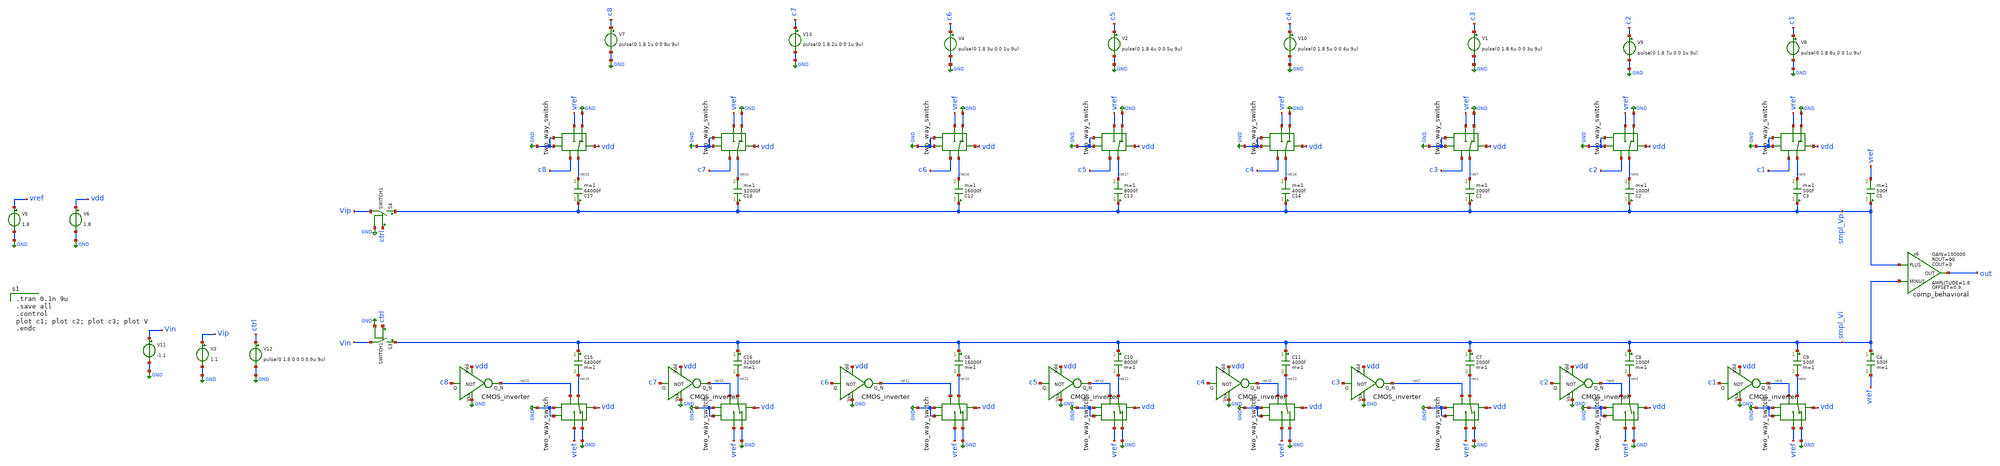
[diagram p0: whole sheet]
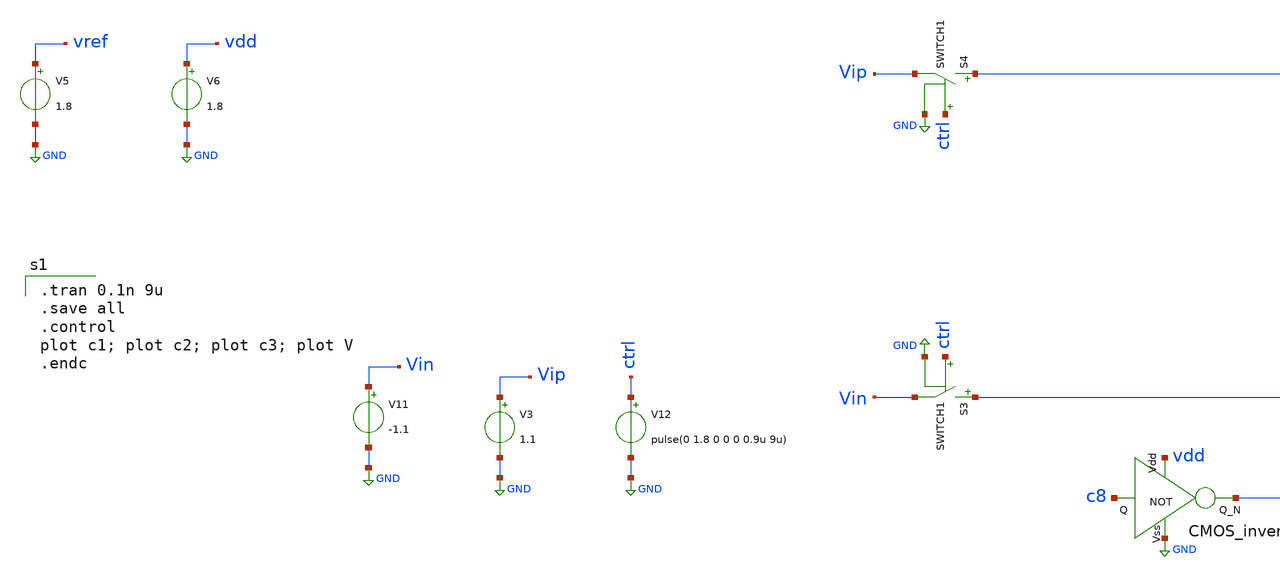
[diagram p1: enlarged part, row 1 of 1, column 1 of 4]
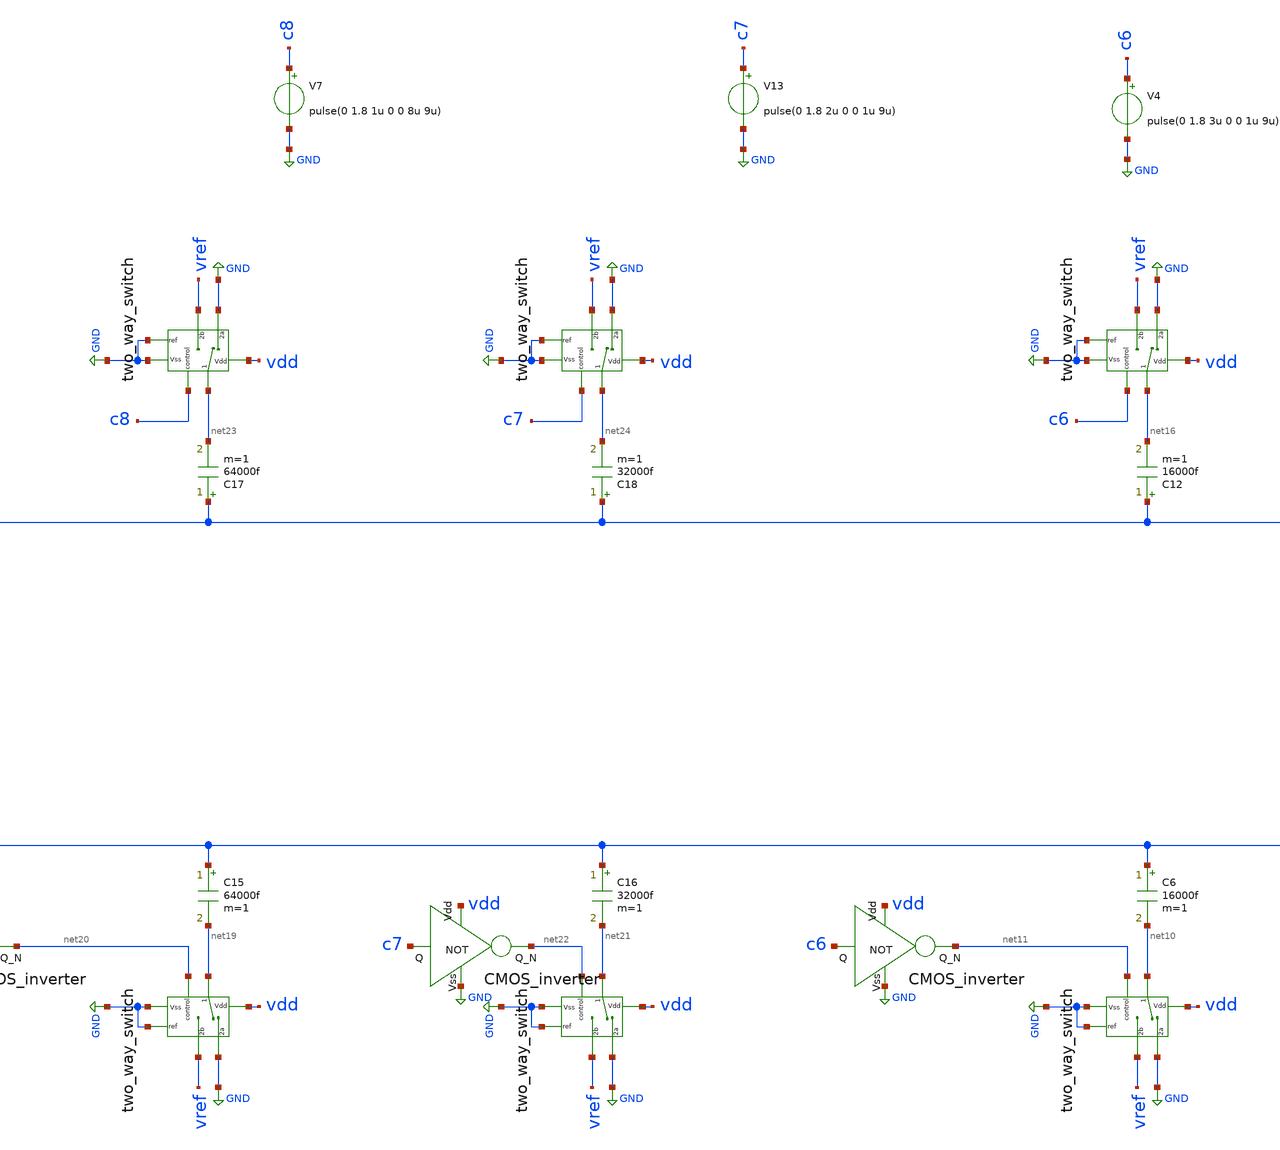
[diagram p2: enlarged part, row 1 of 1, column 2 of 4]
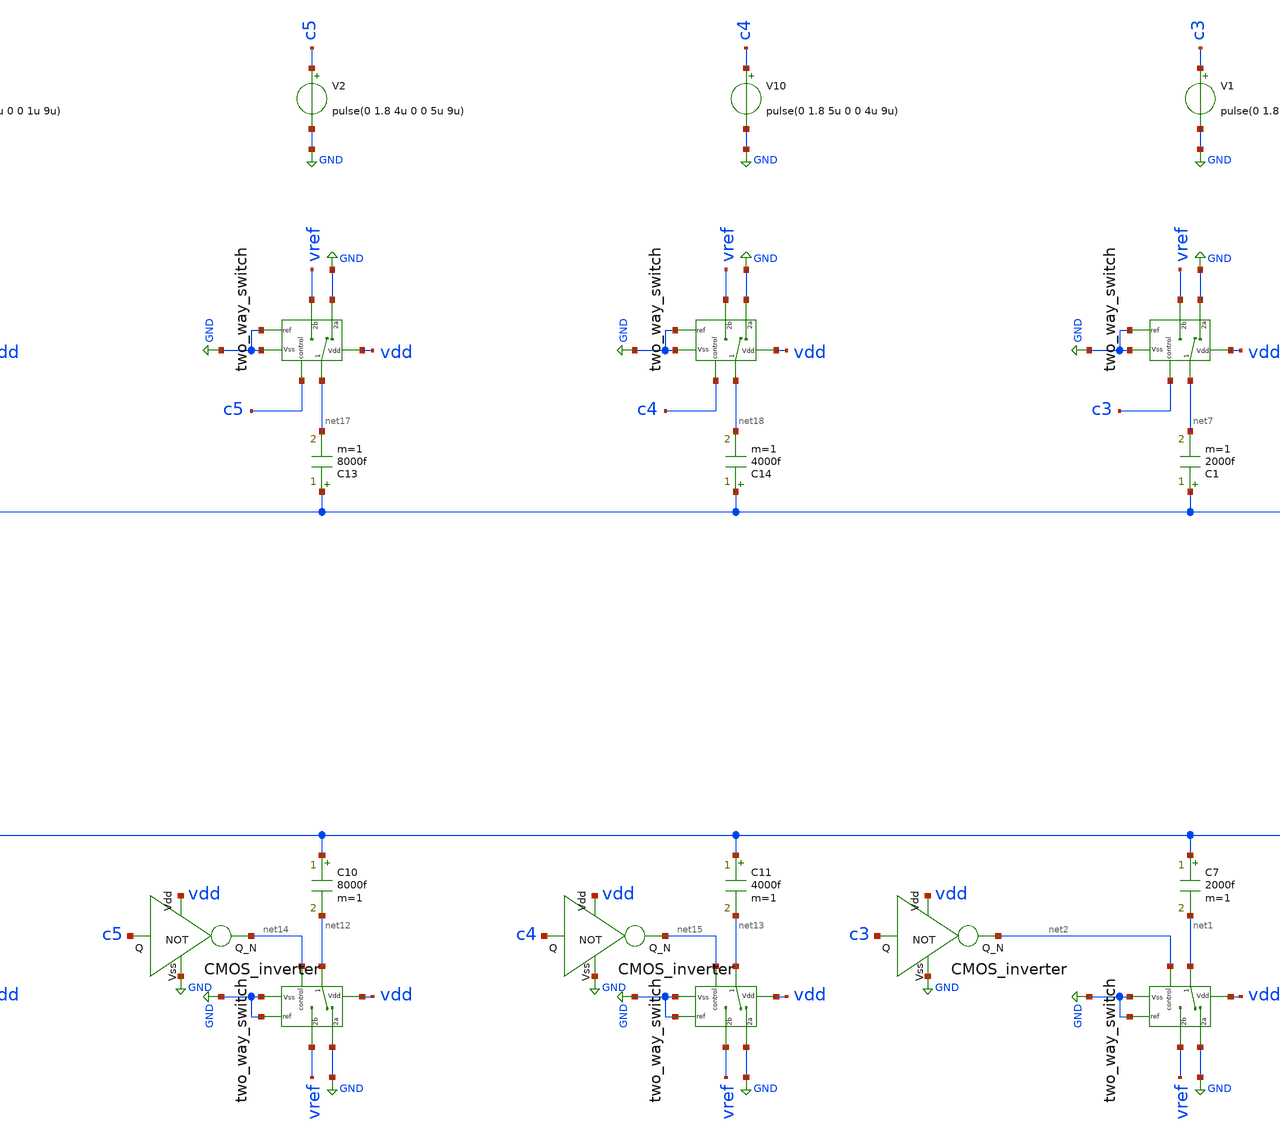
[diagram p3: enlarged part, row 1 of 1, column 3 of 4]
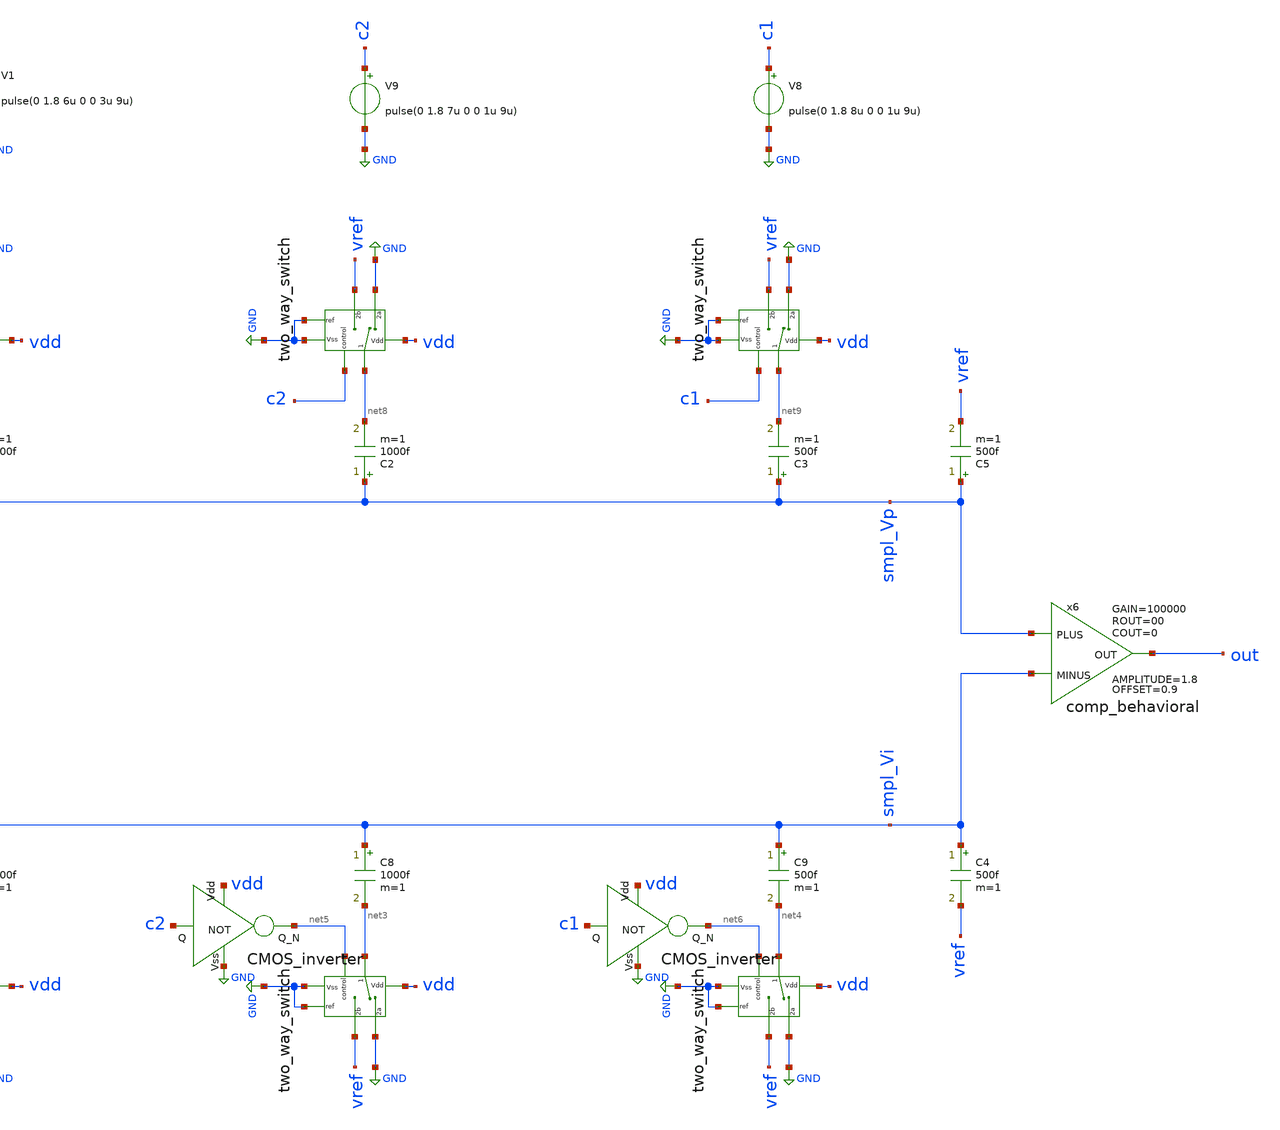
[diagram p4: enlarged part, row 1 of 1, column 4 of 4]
** sch_path: Behavioral_model/diff_mode_behavioral.sch
**.subckt diff_mode_behavioral
S3 smpl_Vi Vin ctrl GND SWITCH1
V12 ctrl GND pulse(0 1.8 0 0 0 0.9u 9u)
V3 Vip GND 1.1
C7 smpl_Vi net1 2000f m=1
x7 net1 vdd net2 GND GND vref GND two_way_switch
C8 smpl_Vi net3 1000f m=1
C9 smpl_Vi net4 500f m=1
x1 net3 vdd net5 GND GND vref GND two_way_switch
x2 net4 vdd net6 GND GND vref GND two_way_switch
V5 vref GND 1.8
V6 vdd GND 1.8
S4 smpl_Vp Vip ctrl GND SWITCH1
C1 smpl_Vp net7 2000f m=1
x3 net7 vdd c3 GND GND vref GND two_way_switch
C2 smpl_Vp net8 1000f m=1
C3 smpl_Vp net9 500f m=1
x4 net8 vdd c2 GND GND vref GND two_way_switch
x5 net9 vdd c1 GND GND vref GND two_way_switch
V8 c1 GND pulse(0 1.8 8u 0 0 1u 9u)
V9 c2 GND pulse(0 1.8 7u 0 0 1u 9u)
V10 c4 GND pulse(0 1.8 5u 0 0 4u 9u)
x6 smpl_Vp smpl_Vi out comp_behavioral OFFSET=0.9 AMPLITUDE=1.8 GAIN=100000 ROUT=00 COUT=0
V11 Vin GND -1.1
C4 smpl_Vi vref 500f m=1
C5 smpl_Vp vref 500f m=1
x8 vdd c3 net2 GND CMOS_inverter
x9 vdd c2 net5 GND CMOS_inverter
x10 vdd c1 net6 GND CMOS_inverter
C6 smpl_Vi net10 16000f m=1
x11 net10 vdd net11 GND GND vref GND two_way_switch
C10 smpl_Vi net12 8000f m=1
C11 smpl_Vi net13 4000f m=1
x12 net12 vdd net14 GND GND vref GND two_way_switch
x13 net13 vdd net15 GND GND vref GND two_way_switch
C12 smpl_Vp net16 16000f m=1
x14 net16 vdd c6 GND GND vref GND two_way_switch
C13 smpl_Vp net17 8000f m=1
C14 smpl_Vp net18 4000f m=1
x15 net17 vdd c5 GND GND vref GND two_way_switch
x16 net18 vdd c4 GND GND vref GND two_way_switch
x17 vdd c6 net11 GND CMOS_inverter
x18 vdd c5 net14 GND CMOS_inverter
x19 vdd c4 net15 GND CMOS_inverter
C15 smpl_Vi net19 64000f m=1
x20 net19 vdd net20 GND GND vref GND two_way_switch
C16 smpl_Vi net21 32000f m=1
x21 net21 vdd net22 GND GND vref GND two_way_switch
C17 smpl_Vp net23 64000f m=1
x22 net23 vdd c8 GND GND vref GND two_way_switch
C18 smpl_Vp net24 32000f m=1
x23 net24 vdd c7 GND GND vref GND two_way_switch
x24 vdd c8 net20 GND CMOS_inverter
x25 vdd c7 net22 GND CMOS_inverter
V1 c3 GND pulse(0 1.8 6u 0 0 3u 9u)
V2 c5 GND pulse(0 1.8 4u 0 0 5u 9u)
V4 c6 GND pulse(0 1.8 3u 0 0 1u 9u)
V7 c8 GND pulse(0 1.8 1u 0 0 8u 9u)
V13 c7 GND pulse(0 1.8 2u 0 0 1u 9u)
**** begin user architecture code

.tran 0.1n 9u
.save all
.control
plot c1; plot c2; plot c3; plot V
.endc


.lib /usr/local/share/pdk/sky130A/libs.tech/ngspice/sky130.lib.spice tt


.model switch1 sw vt=0.1 vh=0 ron=1m roff=100G

**** end user architecture code
**.ends

* expanding   symbol:  two_way_switch.sym # of pins=7
** sym_path: Behavioral_model/two_way_switch.sym
** sch_path: Behavioral_model/two_way_switch.sch
.subckt two_way_switch 1 Vdd control ref 2a 2b Vss
*.ipin 2b
*.ipin 2a
*.ipin ref
*.ipin 1
*.ipin Vdd
*.ipin Vss
*.ipin control
S1 1 2a control ref SWITCH1
S2 1 2b net1 ref SWITCH1
x1 Vdd control net1 Vss CMOS_inverter
.ends


* expanding   symbol:  comp_behavioral.sym # of pins=3
** sym_path: Behavioral_model/comp_behavioral.sym
** sch_path: Behavioral_model/comp_behavioral.sch
.subckt comp_behavioral PLUS MINUS OUT  OFFSET=0.9 AMPLITUDE=0.9 GAIN=100000 ROUT=00 COUT=0
*.ipin PLUS
*.ipin MINUS
*.opin OUT
B1 IOUT 0 V = {OFFSET + AMPLITUDE/2*(tanh(V(IPLUS,IMINUS)*GAIN*2/AMPLITUDE))}
V1 IPLUS PLUS 3
V2 IMINUS MINUS 3
R1 OUT IOUT {ROUT} m=1
C3 OUT 0 {COUT} m=1
.ends


* expanding   symbol:  CMOS_inverter.sym # of pins=4
** sym_path: Behavioral_model/CMOS_inverter.sym
** sch_path: Behavioral_model/CMOS_inverter.sch
.subckt CMOS_inverter Vdd Q Q_N Vss
*.ipin Q
*.ipin Vdd
*.ipin Vss
*.opin Q_N
XM1 Q_N Q Vss Vss sky130_fd_pr__nfet_01v8 L=0.15 W=1 nf=1 ad='int((nf+1)/2) * W/nf * 0.29' as='int((nf+2)/2) * W/nf * 0.29'
+ pd='2*int((nf+1)/2) * (W/nf + 0.29)' ps='2*int((nf+2)/2) * (W/nf + 0.29)' nrd='0.29 / W' nrs='0.29 / W'
+ sa=0 sb=0 sd=0 mult=1 m=1
XM3 Q_N Q Vdd Vdd sky130_fd_pr__pfet_01v8 L=0.15 W=1 nf=1 ad='int((nf+1)/2) * W/nf * 0.29' as='int((nf+2)/2) * W/nf * 0.29'
+ pd='2*int((nf+1)/2) * (W/nf + 0.29)' ps='2*int((nf+2)/2) * (W/nf + 0.29)' nrd='0.29 / W' nrs='0.29 / W'
+ sa=0 sb=0 sd=0 mult=1 m=1
.ends

.GLOBAL GND
.end
